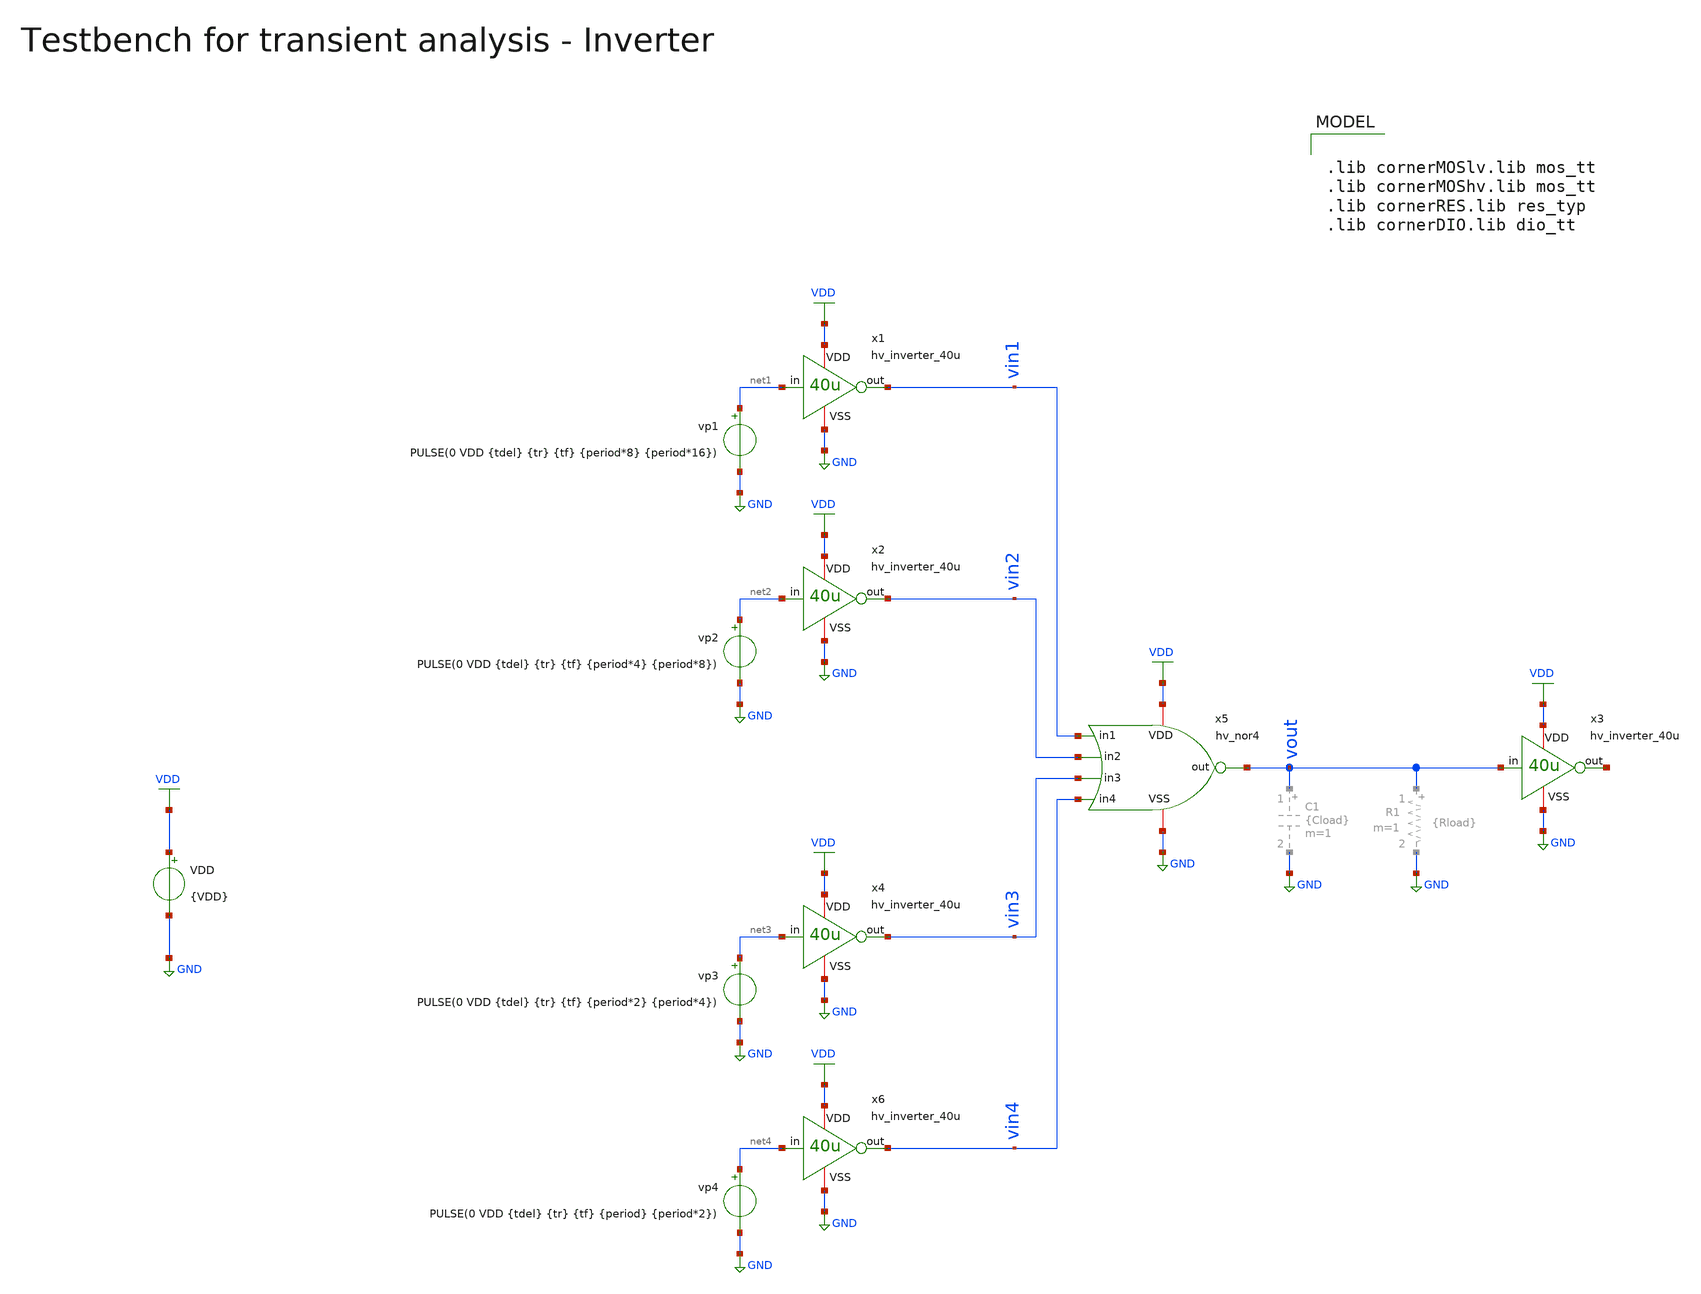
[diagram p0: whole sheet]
** sch_path: macros/heichips26_vcr/macros/switched_capacitor/testbenches/xschem/tb_hv_nor4_tran.sch
**.subckt tb_hv_nor4_tran
VDD VDD GND {VDD}
vp2 net2 GND PULSE(0 VDD {tdel} {tr} {tf} {period*4} {period*8})
vp1 net1 GND PULSE(0 VDD {tdel} {tr} {tf} {period*8} {period*16})
x1 VDD net1 vin1 GND hv_inverter_40u
x2 VDD net2 vin2 GND hv_inverter_40u
x3 VDD vout net5 GND hv_inverter_40u
x5 VDD vin1 vout vin2 GND vin3 vin4 hv_nor4
vp3 net3 GND PULSE(0 VDD {tdel} {tr} {tf} {period*2} {period*4})
x4 VDD net3 vin3 GND hv_inverter_40u
vp4 net4 GND PULSE(0 VDD {tdel} {tr} {tf} {period} {period*2})
x6 VDD net4 vin4 GND hv_inverter_40u
**** begin user architecture code


.param VDD=3.3
.csparam VDD=VDD
.param Vcm=VDD/2
.param temp=27
.param Cload=10p
.param Rload=1k

.param period = 1n
.param tdel   = {period/2}
.param ton    = {period*2}
.csparam tstop  = {17*period}
.csparam tstep  = {period/100}
.param tr     = {period/100}
.param tf     = {period/100}

.options savecurrents klu method=gear reltol=1e-4 abstol=1e-15 gmin=1e-15
.control

save all

* Operating Point Analysis
op
remzerovec
write @schname\.raw
set appendwrite

* Transient Analysis
tran {$&tstep} {$&tstop}
write @schname\.raw

* Plotting
plot vin1+16 vin2+12 vin3+8 vin4+4 vout

* Write Data
unset appendwrite
set wr_vecnames
set wr_singlescale
wrdata ../plot_simulations/data/@schname\.txt v(vin1) v(vin2) v(vout)

*quit
.endc



.lib cornerMOSlv.lib mos_tt
.lib cornerMOShv.lib mos_tt
.lib cornerRES.lib res_typ
.lib cornerDIO.lib dio_tt

**** end user architecture code
**.ends

* expanding   symbol:  hv_inverter_40u.sym # of pins=4
** sym_path: macros/heichips26_vcr/macros/switched_capacitor/schematic/xschem/hv_inverter_40u.sym
** sch_path: macros/heichips26_vcr/macros/switched_capacitor/schematic/xschem/hv_inverter_40u.sch
.subckt hv_inverter_40u VDD in out VSS
*.ipin in
*.iopin VDD
*.iopin VSS
*.opin out
XM2 out in VSS VSS sg13_hv_nmos w={n_w} l={n_l} ng={ng} m=1 mm_ok=1
XM3 out in VDD VDD sg13_hv_pmos w={p_w} l={p_l} ng={ng} m=1 mm_ok=1
**** begin user architecture code


.param w   = 10u
.param ng  = 4
.param n_ng = ng
.param n_w = {3u*n_ng}
.param n_l = 0.45u
.param p_ng = ng
.param p_w = {10u*p_ng}
.param p_l = 0.4u


**** end user architecture code
.ends


* expanding   symbol:  hv_nor4.sym # of pins=7
** sym_path: macros/heichips26_vcr/macros/switched_capacitor/schematic/xschem/hv_nor4.sym
** sch_path: macros/heichips26_vcr/macros/switched_capacitor/schematic/xschem/hv_nor4.sch
.subckt hv_nor4 VDD in1 out in2 VSS in3 in4
*.ipin in1
*.iopin VDD
*.iopin VSS
*.opin out
*.ipin in2
*.ipin in3
*.ipin in4
**** begin user architecture code


.param w   = 10u
.param ng  = 4
.param n_ng = ng
.param n_w = {3u*n_ng}
.param n_l = 0.45u
.param p_ng = ng
.param p_w = {10u*p_ng}
.param p_l = 0.4u


**** end user architecture code
XM2 out in2 VSS VSS sg13_hv_nmos w={n_w} l={n_l} ng={ng} m=1 mm_ok=1
XM3 net3 in1 VDD VDD sg13_hv_pmos w={p_w} l={p_l} ng={ng} m=1 mm_ok=1
XM1 out in1 VSS VSS sg13_hv_nmos w={n_w} l={n_l} ng={ng} m=1 mm_ok=1
XM4 out in4 net1 VDD sg13_hv_pmos w={p_w} l={p_l} ng={ng} m=1 mm_ok=1
XM5 out in3 VSS VSS sg13_hv_nmos w={n_w} l={n_l} ng={ng} m=1 mm_ok=1
XM6 out in4 VSS VSS sg13_hv_nmos w={n_w} l={n_l} ng={ng} m=1 mm_ok=1
XM7 net1 in4 net2 VDD sg13_hv_pmos w={p_w} l={p_l} ng={ng} m=1 mm_ok=1
XM8 net2 in4 net3 VDD sg13_hv_pmos w={p_w} l={p_l} ng={ng} m=1 mm_ok=1
.ends

.GLOBAL GND
.GLOBAL VDD
.end
